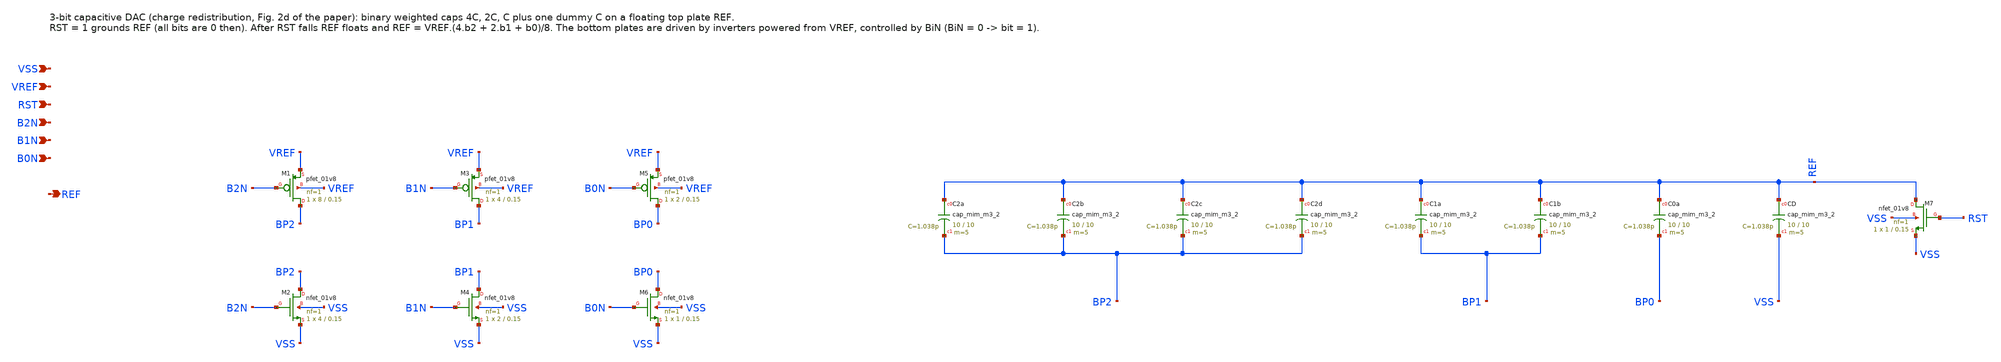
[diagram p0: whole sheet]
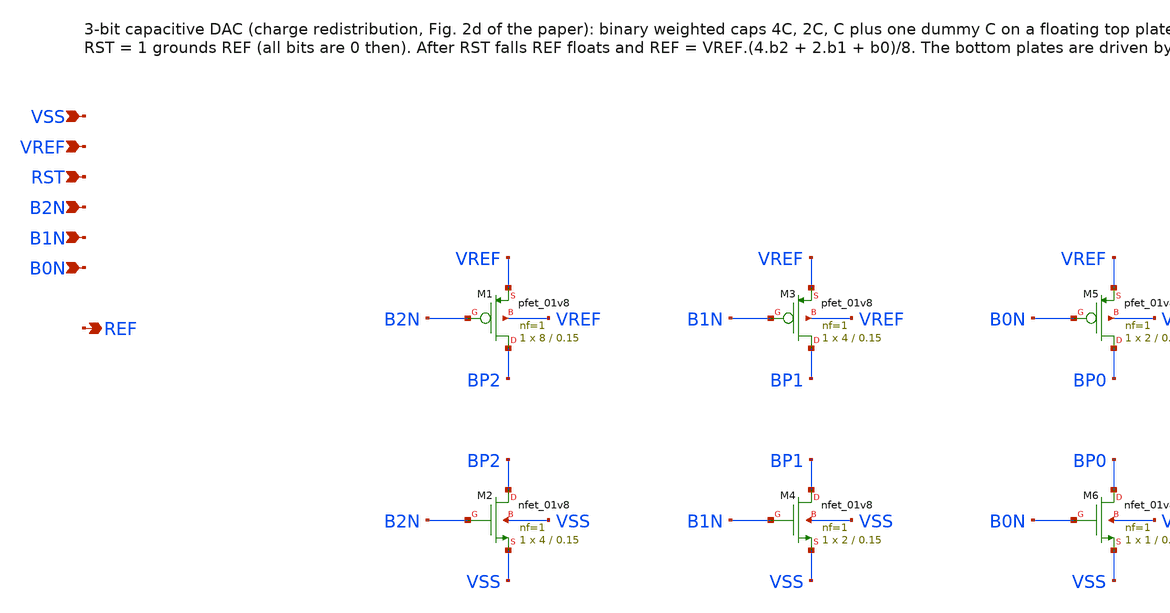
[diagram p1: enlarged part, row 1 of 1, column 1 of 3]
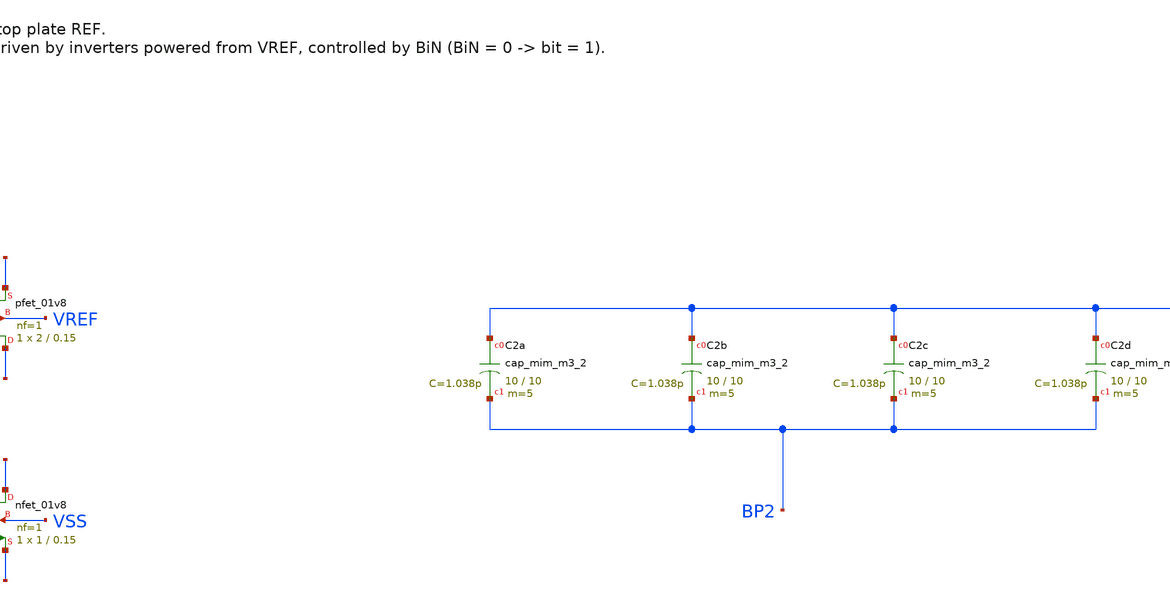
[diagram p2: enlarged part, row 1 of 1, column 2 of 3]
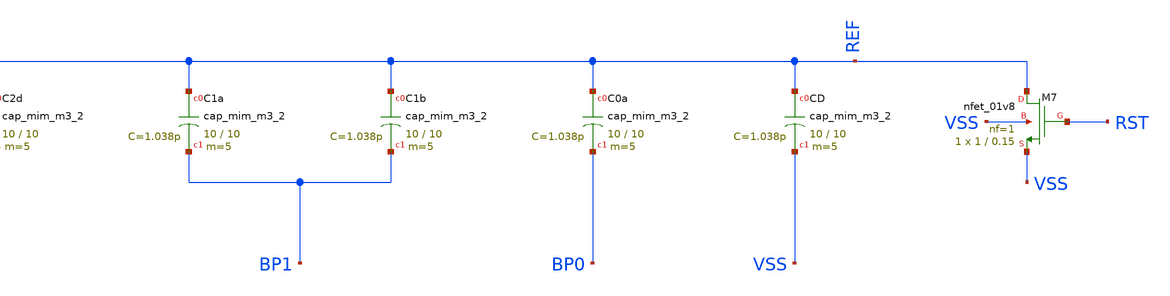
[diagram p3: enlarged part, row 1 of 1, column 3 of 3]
** sch_path: cdac3.sch
**.subckt cdac3 VSS VREF RST B2N B1N B0N REF
*.ipin VSS
*.ipin VREF
*.ipin RST
*.ipin B2N
*.ipin B1N
*.ipin B0N
*.opin REF
XM1 BP2 B2N VREF VREF sky130_fd_pr__pfet_01v8 L=0.15 W=8 nf=1 ad='int((nf+1)/2) * W/nf * 0.29' as='int((nf+2)/2) * W/nf * 0.29'
+ pd='2*int((nf+1)/2) * (W/nf + 0.29)' ps='2*int((nf+2)/2) * (W/nf + 0.29)' nrd='0.29 / W' nrs='0.29 / W'
+ sa=0 sb=0 sd=0 mult=1 m=1
XM2 BP2 B2N VSS VSS sky130_fd_pr__nfet_01v8 L=0.15 W=4 nf=1 ad='int((nf+1)/2) * W/nf * 0.29' as='int((nf+2)/2) * W/nf * 0.29'
+ pd='2*int((nf+1)/2) * (W/nf + 0.29)' ps='2*int((nf+2)/2) * (W/nf + 0.29)' nrd='0.29 / W' nrs='0.29 / W'
+ sa=0 sb=0 sd=0 mult=1 m=1
XM3 BP1 B1N VREF VREF sky130_fd_pr__pfet_01v8 L=0.15 W=4 nf=1 ad='int((nf+1)/2) * W/nf * 0.29' as='int((nf+2)/2) * W/nf * 0.29'
+ pd='2*int((nf+1)/2) * (W/nf + 0.29)' ps='2*int((nf+2)/2) * (W/nf + 0.29)' nrd='0.29 / W' nrs='0.29 / W'
+ sa=0 sb=0 sd=0 mult=1 m=1
XM4 BP1 B1N VSS VSS sky130_fd_pr__nfet_01v8 L=0.15 W=2 nf=1 ad='int((nf+1)/2) * W/nf * 0.29' as='int((nf+2)/2) * W/nf * 0.29'
+ pd='2*int((nf+1)/2) * (W/nf + 0.29)' ps='2*int((nf+2)/2) * (W/nf + 0.29)' nrd='0.29 / W' nrs='0.29 / W'
+ sa=0 sb=0 sd=0 mult=1 m=1
XM5 BP0 B0N VREF VREF sky130_fd_pr__pfet_01v8 L=0.15 W=2 nf=1 ad='int((nf+1)/2) * W/nf * 0.29' as='int((nf+2)/2) * W/nf * 0.29'
+ pd='2*int((nf+1)/2) * (W/nf + 0.29)' ps='2*int((nf+2)/2) * (W/nf + 0.29)' nrd='0.29 / W' nrs='0.29 / W'
+ sa=0 sb=0 sd=0 mult=1 m=1
XM6 BP0 B0N VSS VSS sky130_fd_pr__nfet_01v8 L=0.15 W=1 nf=1 ad='int((nf+1)/2) * W/nf * 0.29' as='int((nf+2)/2) * W/nf * 0.29'
+ pd='2*int((nf+1)/2) * (W/nf + 0.29)' ps='2*int((nf+2)/2) * (W/nf + 0.29)' nrd='0.29 / W' nrs='0.29 / W'
+ sa=0 sb=0 sd=0 mult=1 m=1
XC2a REF BP2 sky130_fd_pr__cap_mim_m3_2 W=10 L=10 MF=5 m=5
XC2b REF BP2 sky130_fd_pr__cap_mim_m3_2 W=10 L=10 MF=5 m=5
XC2c REF BP2 sky130_fd_pr__cap_mim_m3_2 W=10 L=10 MF=5 m=5
XC2d REF BP2 sky130_fd_pr__cap_mim_m3_2 W=10 L=10 MF=5 m=5
XC1a REF BP1 sky130_fd_pr__cap_mim_m3_2 W=10 L=10 MF=5 m=5
XC1b REF BP1 sky130_fd_pr__cap_mim_m3_2 W=10 L=10 MF=5 m=5
XC0a REF BP0 sky130_fd_pr__cap_mim_m3_2 W=10 L=10 MF=5 m=5
XCD REF VSS sky130_fd_pr__cap_mim_m3_2 W=10 L=10 MF=5 m=5
XM7 REF RST VSS VSS sky130_fd_pr__nfet_01v8 L=0.15 W=1 nf=1 ad='int((nf+1)/2) * W/nf * 0.29' as='int((nf+2)/2) * W/nf * 0.29'
+ pd='2*int((nf+1)/2) * (W/nf + 0.29)' ps='2*int((nf+2)/2) * (W/nf + 0.29)' nrd='0.29 / W' nrs='0.29 / W'
+ sa=0 sb=0 sd=0 mult=1 m=1
**.ends
.end
